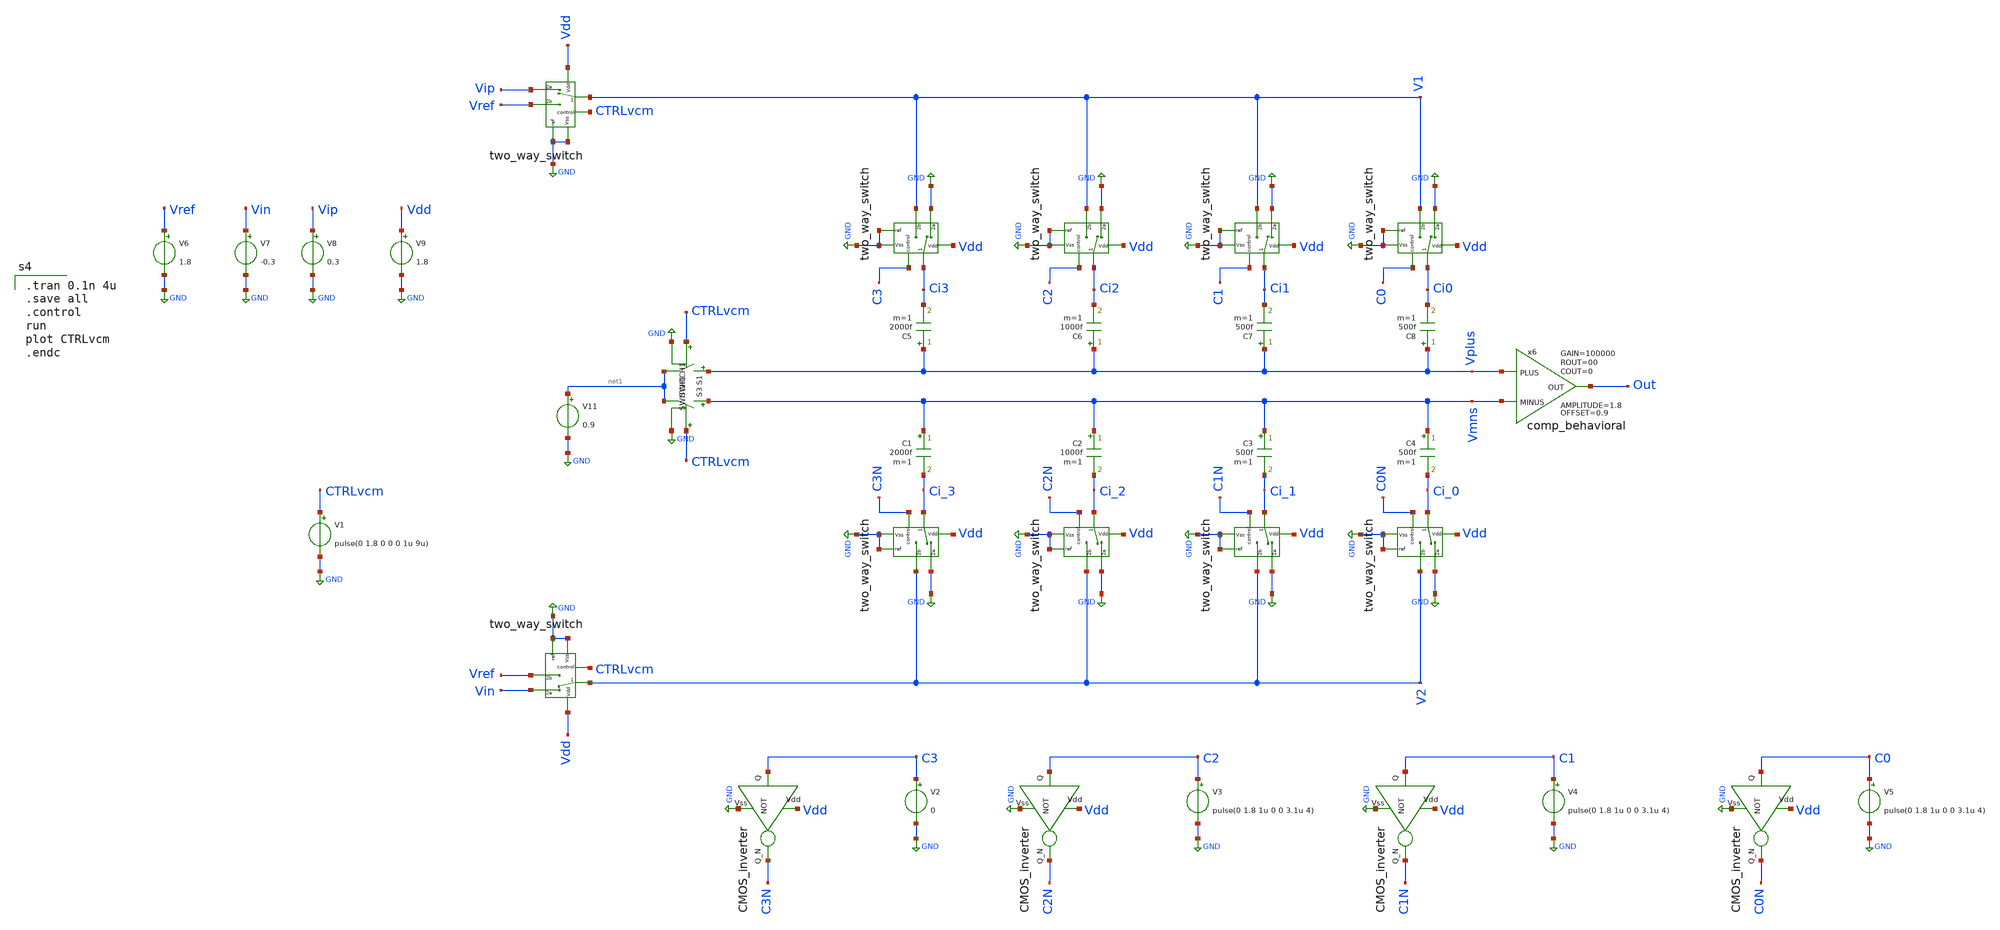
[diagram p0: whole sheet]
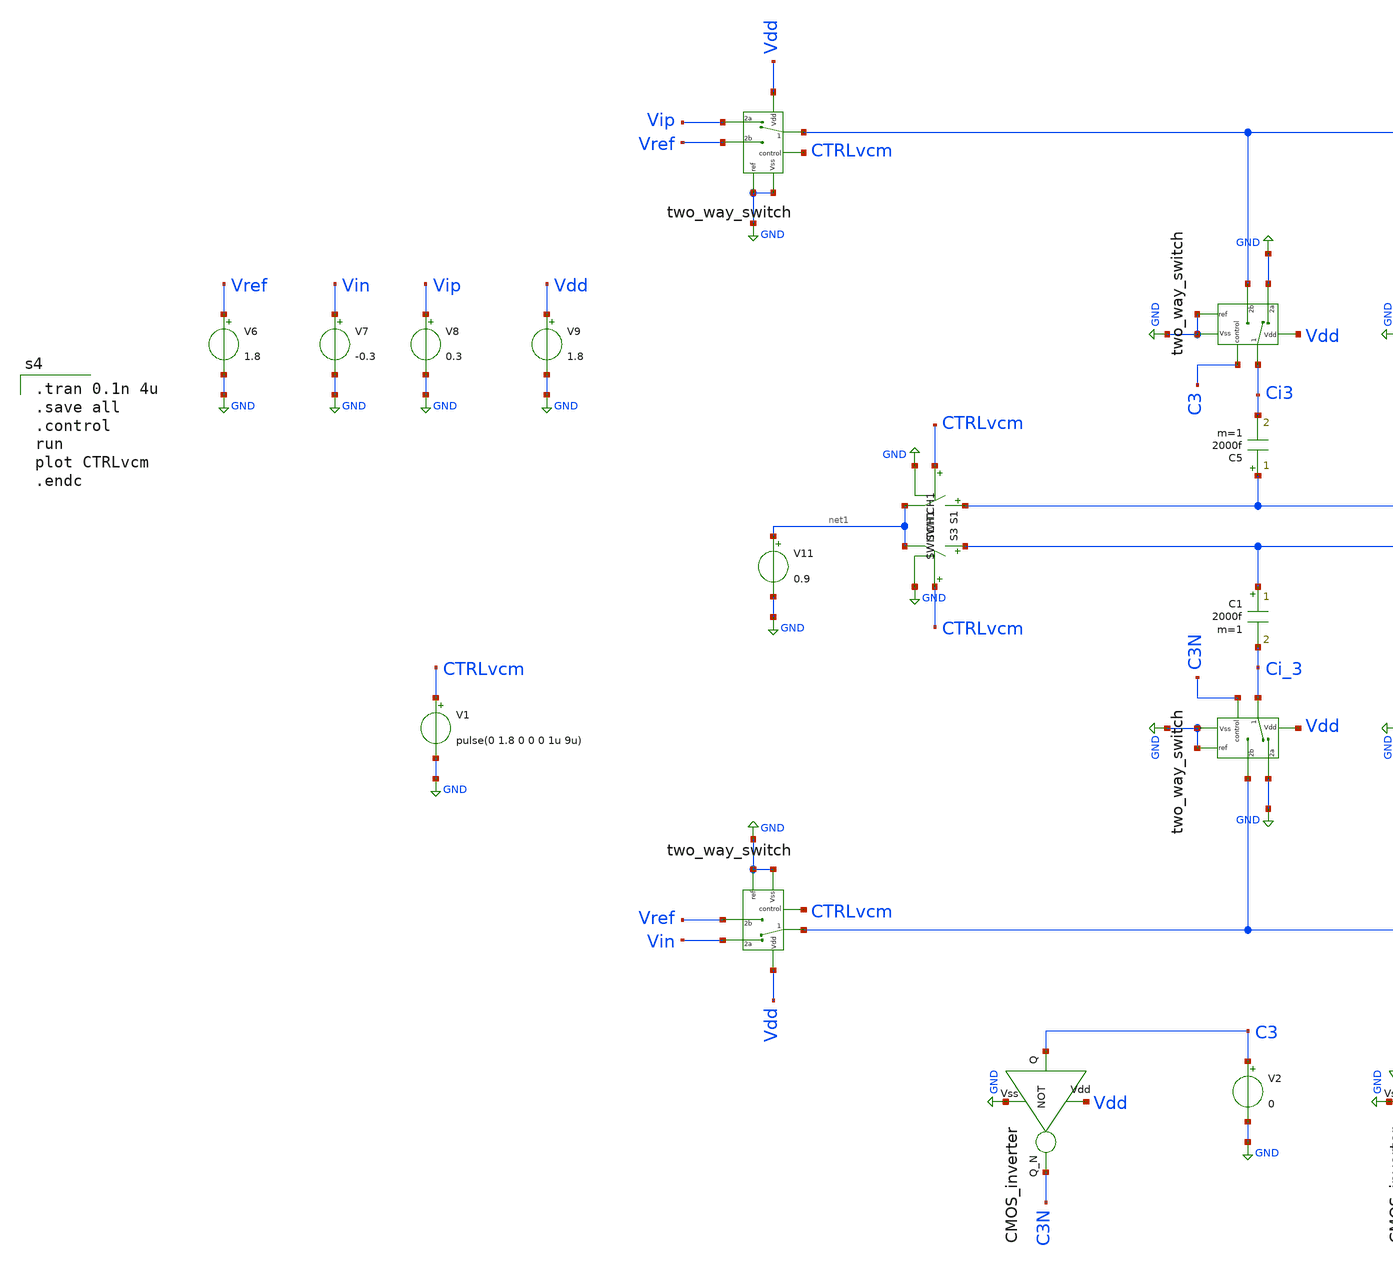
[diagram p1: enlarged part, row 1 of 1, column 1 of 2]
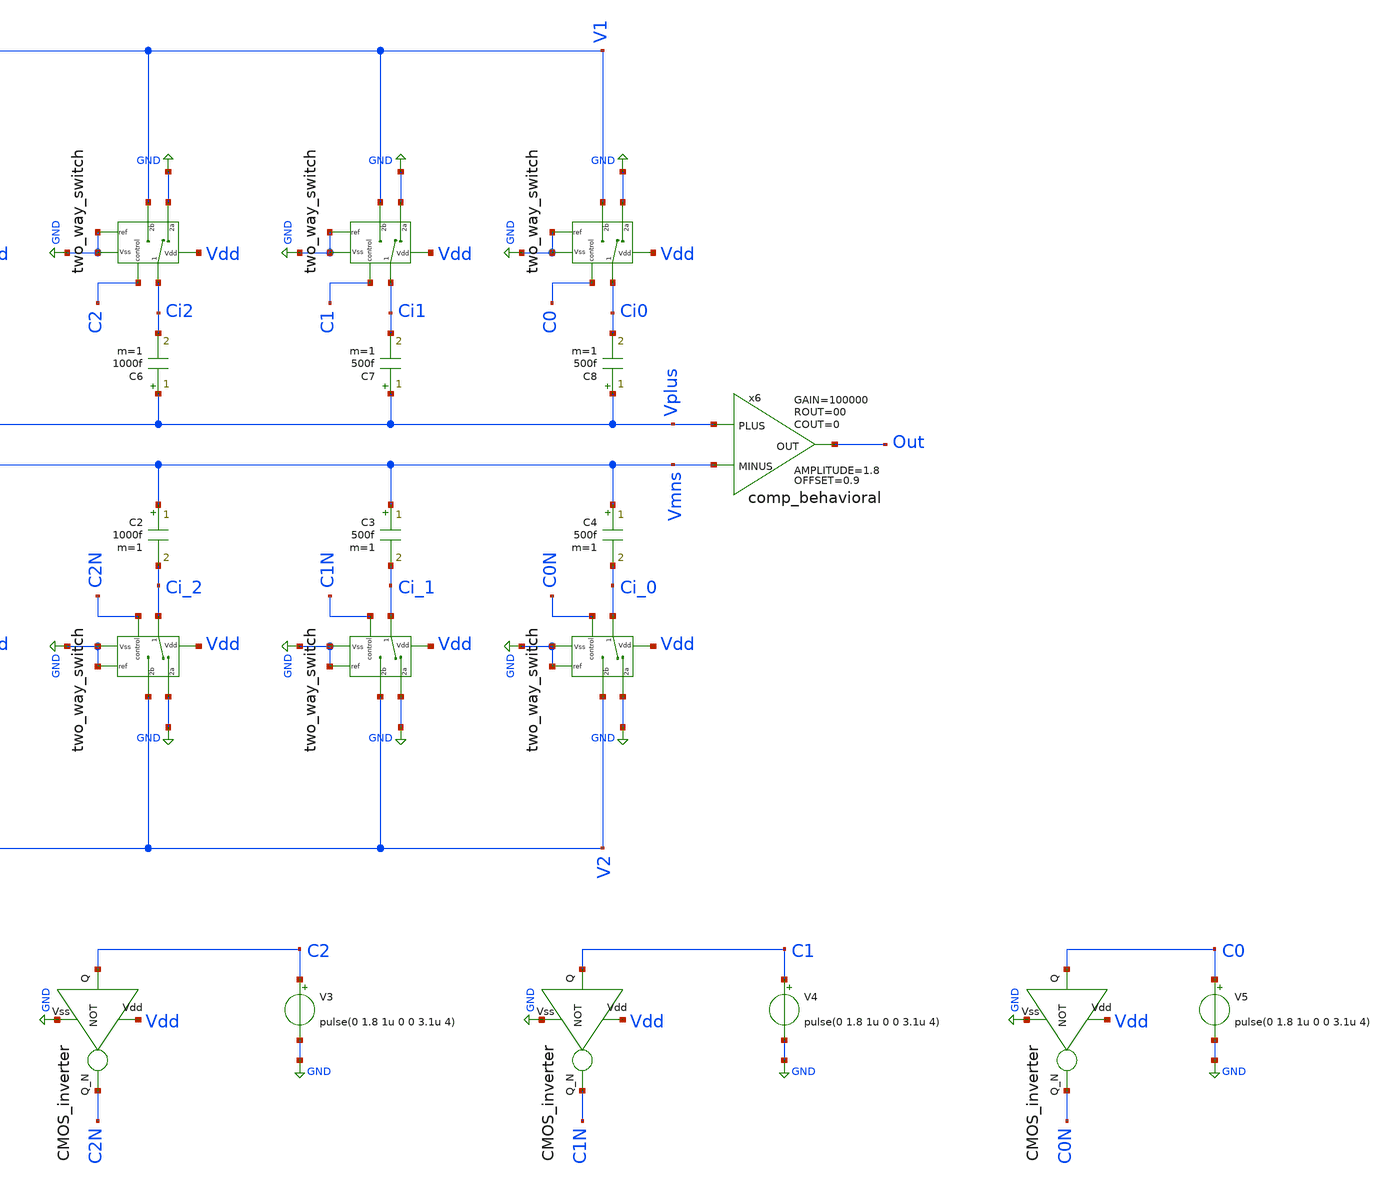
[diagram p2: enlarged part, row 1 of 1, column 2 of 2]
** sch_path: Behavioral_model/testing.sch
**.subckt testing
x6 Vplus Vmns Out comp_behavioral OFFSET=0.9 AMPLITUDE=1.8 GAIN=100000 ROUT=00 COUT=0
V11 net1 GND 0.9
C1 Vmns Ci_3 2000f m=1
C2 Vmns Ci_2 1000f m=1
C3 Vmns Ci_1 500f m=1
C4 Vmns Ci_0 500f m=1
C5 Vplus Ci3 2000f m=1
C6 Vplus Ci2 1000f m=1
C7 Vplus Ci1 500f m=1
C8 Vplus Ci0 500f m=1
x9 Ci0 Vdd C0 GND GND V1 GND two_way_switch
S1 Vplus net1 CTRLvcm GND SWITCH1
S3 Vmns net1 CTRLvcm GND SWITCH1
V1 CTRLvcm GND pulse(0 1.8 0 0 0 1u 9u)
x11 V1 Vdd CTRLvcm GND Vip Vref GND two_way_switch
x5 Ci1 Vdd C1 GND GND V1 GND two_way_switch
x7 Ci2 Vdd C2 GND GND V1 GND two_way_switch
x8 Ci3 Vdd C3 GND GND V1 GND two_way_switch
x1 Ci_0 Vdd C0N GND GND V2 GND two_way_switch
x2 V2 Vdd CTRLvcm GND Vin Vref GND two_way_switch
x3 Ci_1 Vdd C1N GND GND V2 GND two_way_switch
x4 Ci_2 Vdd C2N GND GND V2 GND two_way_switch
x10 Ci_3 Vdd C3N GND GND V2 GND two_way_switch
V2 C3 GND 0
V3 C2 GND pulse(0 1.8 1u 0 0 3.1u 4)
V4 C1 GND pulse(0 1.8 1u 0 0 3.1u 4)
V5 C0 GND pulse(0 1.8 1u 0 0 3.1u 4)
V6 Vref GND 1.8
V7 Vin GND -0.3
V8 Vip GND 0.3
V9 Vdd GND 1.8
x12 Vdd C3 C3N GND CMOS_inverter
x13 Vdd C2 C2N GND CMOS_inverter
x14 Vdd C1 C1N GND CMOS_inverter
x15 Vdd C0 C0N GND CMOS_inverter
**** begin user architecture code

.lib /usr/local/share/pdk/sky130A/libs.tech/ngspice/sky130.lib.spice tt


.model switch1 sw vt=0.1 vh=0 ron=1m roff=100G


.tran 0.1n 4u
.save all
.control
run
plot CTRLvcm
.endc

**** end user architecture code
**.ends

* expanding   symbol:  comp_behavioral.sym # of pins=3
** sym_path: Behavioral_model/comp_behavioral.sym
** sch_path: Behavioral_model/comp_behavioral.sch
.subckt comp_behavioral PLUS MINUS OUT  OFFSET=0.9 AMPLITUDE=0.9 GAIN=100000 ROUT=00 COUT=0
*.ipin PLUS
*.ipin MINUS
*.opin OUT
B1 IOUT 0 V = {OFFSET + AMPLITUDE/2*(tanh(V(IPLUS,IMINUS)*GAIN*2/AMPLITUDE))}
V1 IPLUS PLUS 3
V2 IMINUS MINUS 3
R1 OUT IOUT {ROUT} m=1
C3 OUT 0 {COUT} m=1
.ends


* expanding   symbol:  two_way_switch.sym # of pins=7
** sym_path: Behavioral_model/two_way_switch.sym
** sch_path: Behavioral_model/two_way_switch.sch
.subckt two_way_switch 1 Vdd control ref 2a 2b Vss
*.iopin 2b
*.iopin 2a
*.ipin ref
*.iopin 1
*.ipin Vdd
*.ipin Vss
*.ipin control
S1 1 2a control ref SWITCH1
S2 1 2b net1 ref SWITCH1
x1 Vdd control net1 Vss CMOS_inverter
.ends


* expanding   symbol:  CMOS_inverter.sym # of pins=4
** sym_path: Behavioral_model/CMOS_inverter.sym
** sch_path: Behavioral_model/CMOS_inverter.sch
.subckt CMOS_inverter Vdd Q Q_N Vss
*.ipin Q
*.ipin Vdd
*.ipin Vss
*.opin Q_N
XM1 Q_N Q Vss Vss sky130_fd_pr__nfet_01v8 L=0.15 W=1 nf=1 ad='int((nf+1)/2) * W/nf * 0.29' as='int((nf+2)/2) * W/nf * 0.29'
+ pd='2*int((nf+1)/2) * (W/nf + 0.29)' ps='2*int((nf+2)/2) * (W/nf + 0.29)' nrd='0.29 / W' nrs='0.29 / W'
+ sa=0 sb=0 sd=0 mult=1 m=1
XM3 Q_N Q Vdd Vdd sky130_fd_pr__pfet_01v8 L=0.15 W=1 nf=1 ad='int((nf+1)/2) * W/nf * 0.29' as='int((nf+2)/2) * W/nf * 0.29'
+ pd='2*int((nf+1)/2) * (W/nf + 0.29)' ps='2*int((nf+2)/2) * (W/nf + 0.29)' nrd='0.29 / W' nrs='0.29 / W'
+ sa=0 sb=0 sd=0 mult=1 m=1
.ends

.GLOBAL GND
.end
